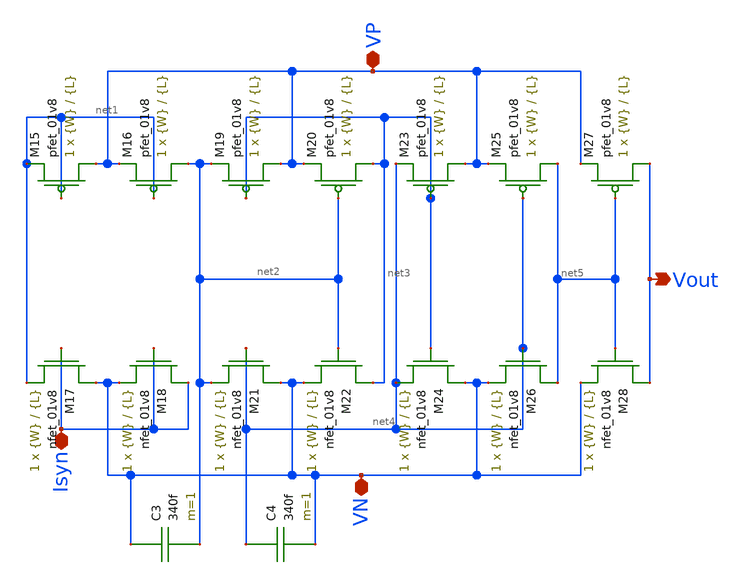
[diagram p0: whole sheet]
** sch_path: schematic/besrour_neuron_cm_lds.sch
**.subckt besrour_neuron_cm_lds VP VN Isyn Vout
*.iopin VP
*.iopin VN
*.iopin Isyn
*.opin Vout
XM15 VP net1 net1 VDD sky130_fd_pr__pfet_01v8 L={L} W={W} nf=1 ad='int((nf+1)/2) * W/nf * 0.29' as='int((nf+2)/2) * W/nf * 0.29'
+ pd='2*int((nf+1)/2) * (W/nf + 0.29)' ps='2*int((nf+2)/2) * (W/nf + 0.29)' nrd='0.29 / W' nrs='0.29 / W'
+ sa=0 sb=0 sd=0 mult=1 m=1
XM16 net2 net1 VP VDD sky130_fd_pr__pfet_01v8 L={L} W={W} nf=1 ad='int((nf+1)/2) * W/nf * 0.29' as='int((nf+2)/2) * W/nf * 0.29'
+ pd='2*int((nf+1)/2) * (W/nf + 0.29)' ps='2*int((nf+2)/2) * (W/nf + 0.29)' nrd='0.29 / W' nrs='0.29 / W'
+ sa=0 sb=0 sd=0 mult=1 m=1
XM17 VN Isyn net1 GND sky130_fd_pr__nfet_01v8 L={L} W={W} nf=1 ad='int((nf+1)/2) * W/nf * 0.29' as='int((nf+2)/2) * W/nf * 0.29'
+ pd='2*int((nf+1)/2) * (W/nf + 0.29)' ps='2*int((nf+2)/2) * (W/nf + 0.29)' nrd='0.29 / W' nrs='0.29 / W'
+ sa=0 sb=0 sd=0 mult=1 m=1
XM18 Isyn Isyn VN GND sky130_fd_pr__nfet_01v8 L={L} W={W} nf=1 ad='int((nf+1)/2) * W/nf * 0.29' as='int((nf+2)/2) * W/nf * 0.29'
+ pd='2*int((nf+1)/2) * (W/nf + 0.29)' ps='2*int((nf+2)/2) * (W/nf + 0.29)' nrd='0.29 / W' nrs='0.29 / W'
+ sa=0 sb=0 sd=0 mult=1 m=1
XM19 VP net3 net2 VDD sky130_fd_pr__pfet_01v8 L={L} W={W} nf=1 ad='int((nf+1)/2) * W/nf * 0.29' as='int((nf+2)/2) * W/nf * 0.29'
+ pd='2*int((nf+1)/2) * (W/nf + 0.29)' ps='2*int((nf+2)/2) * (W/nf + 0.29)' nrd='0.29 / W' nrs='0.29 / W'
+ sa=0 sb=0 sd=0 mult=1 m=1
XM20 net3 net2 VP VDD sky130_fd_pr__pfet_01v8 L={L} W={W} nf=1 ad='int((nf+1)/2) * W/nf * 0.29' as='int((nf+2)/2) * W/nf * 0.29'
+ pd='2*int((nf+1)/2) * (W/nf + 0.29)' ps='2*int((nf+2)/2) * (W/nf + 0.29)' nrd='0.29 / W' nrs='0.29 / W'
+ sa=0 sb=0 sd=0 mult=1 m=1
XM21 VN net4 net2 GND sky130_fd_pr__nfet_01v8 L={L} W={W} nf=1 ad='int((nf+1)/2) * W/nf * 0.29' as='int((nf+2)/2) * W/nf * 0.29'
+ pd='2*int((nf+1)/2) * (W/nf + 0.29)' ps='2*int((nf+2)/2) * (W/nf + 0.29)' nrd='0.29 / W' nrs='0.29 / W'
+ sa=0 sb=0 sd=0 mult=1 m=1
XM22 net3 net2 VN GND sky130_fd_pr__nfet_01v8 L={L} W={W} nf=1 ad='int((nf+1)/2) * W/nf * 0.29' as='int((nf+2)/2) * W/nf * 0.29'
+ pd='2*int((nf+1)/2) * (W/nf + 0.29)' ps='2*int((nf+2)/2) * (W/nf + 0.29)' nrd='0.29 / W' nrs='0.29 / W'
+ sa=0 sb=0 sd=0 mult=1 m=1
XM23 VP net3 net4 VDD sky130_fd_pr__pfet_01v8 L={L} W={W} nf=1 ad='int((nf+1)/2) * W/nf * 0.29' as='int((nf+2)/2) * W/nf * 0.29'
+ pd='2*int((nf+1)/2) * (W/nf + 0.29)' ps='2*int((nf+2)/2) * (W/nf + 0.29)' nrd='0.29 / W' nrs='0.29 / W'
+ sa=0 sb=0 sd=0 mult=1 m=1
XM24 VN net3 net4 GND sky130_fd_pr__nfet_01v8 L={L} W={W} nf=1 ad='int((nf+1)/2) * W/nf * 0.29' as='int((nf+2)/2) * W/nf * 0.29'
+ pd='2*int((nf+1)/2) * (W/nf + 0.29)' ps='2*int((nf+2)/2) * (W/nf + 0.29)' nrd='0.29 / W' nrs='0.29 / W'
+ sa=0 sb=0 sd=0 mult=1 m=1
XM25 net5 net4 VP VDD sky130_fd_pr__pfet_01v8 L={L} W={W} nf=1 ad='int((nf+1)/2) * W/nf * 0.29' as='int((nf+2)/2) * W/nf * 0.29'
+ pd='2*int((nf+1)/2) * (W/nf + 0.29)' ps='2*int((nf+2)/2) * (W/nf + 0.29)' nrd='0.29 / W' nrs='0.29 / W'
+ sa=0 sb=0 sd=0 mult=1 m=1
XM26 net5 net4 VN GND sky130_fd_pr__nfet_01v8 L={L} W={W} nf=1 ad='int((nf+1)/2) * W/nf * 0.29' as='int((nf+2)/2) * W/nf * 0.29'
+ pd='2*int((nf+1)/2) * (W/nf + 0.29)' ps='2*int((nf+2)/2) * (W/nf + 0.29)' nrd='0.29 / W' nrs='0.29 / W'
+ sa=0 sb=0 sd=0 mult=1 m=1
XM27 Vout net5 VP VDD sky130_fd_pr__pfet_01v8 L={L} W={W} nf=1 ad='int((nf+1)/2) * W/nf * 0.29' as='int((nf+2)/2) * W/nf * 0.29'
+ pd='2*int((nf+1)/2) * (W/nf + 0.29)' ps='2*int((nf+2)/2) * (W/nf + 0.29)' nrd='0.29 / W' nrs='0.29 / W'
+ sa=0 sb=0 sd=0 mult=1 m=1
XM28 Vout net5 VN GND sky130_fd_pr__nfet_01v8 L={L} W={W} nf=1 ad='int((nf+1)/2) * W/nf * 0.29' as='int((nf+2)/2) * W/nf * 0.29'
+ pd='2*int((nf+1)/2) * (W/nf + 0.29)' ps='2*int((nf+2)/2) * (W/nf + 0.29)' nrd='0.29 / W' nrs='0.29 / W'
+ sa=0 sb=0 sd=0 mult=1 m=1
C3 VN net2 340f m=1
C4 net4 VN 340f m=1
**.ends
.end
